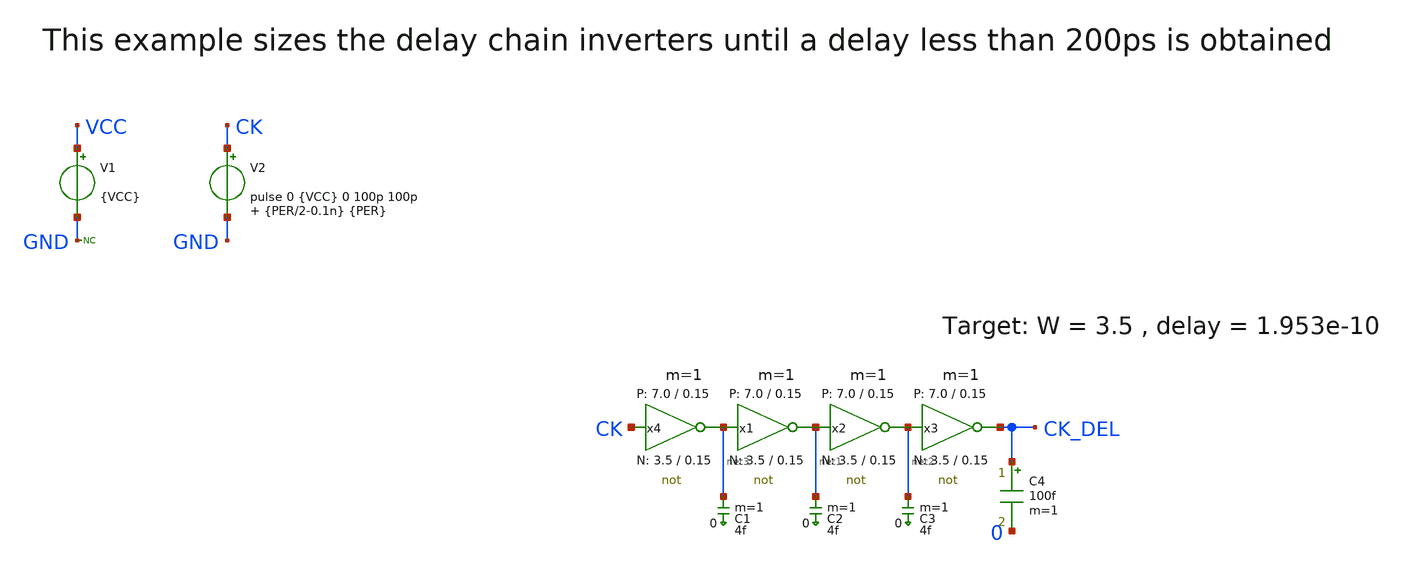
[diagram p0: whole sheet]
** sch_path: sky130A/xschem_libs/sky130_tests/optimize_delay/schematic/optimize_delay.sch
* StefanSchippers/xschem_sky130/sky130_tests/not.sch:
* Copyright 2021 Stefan Frederik Schippers
* Licensed under the Apache License, Version 2.0 (the "License");
.lib $::SKYWATER_MODELS/sky130.lib.spice tt
.include $::SKYWATER_STDCELLS/sky130_fd_sc_hd.spice

**.subckt optimize_delay
V1 VCC GND {VCC}
V2 CK GND pulse 0 {VCC} 0 100p 100p {PER/2-0.1n} {PER}
* noconn GND
C1 net3 0 4f m=1
C2 net1 0 4f m=1
C3 net2 0 4f m=1
x4 net3 CK VCC GND not W_N=3.5 L_N=0.15 W_P=7.0 L_P=0.15 m=1
x1 net1 net3 VCC GND not W_N=3.5 L_N=0.15 W_P=7.0 L_P=0.15 m=1
x2 net2 net1 VCC GND not W_N=3.5 L_N=0.15 W_P=7.0 L_P=0.15 m=1
x3 CK_DEL net2 VCC GND not W_N=3.5 L_N=0.15 W_P=7.0 L_P=0.15 m=1
C4 CK_DEL 0 100f m=1
**** begin user architecture code


.param VCC=1.8
.param FREQ=100e6
.param PER={1/FREQ}
.param ILOAD=100u
.control
  save all
  set nobreak
  set numdgt=3
  set wr_singlescale
  set wr_vecnames
  tran 4p 11n
  write optimize_delay.raw
  * wrdata result.txt ck ck_del
  meas tran del
  + TRIG v(CK) TD=9n VAL=0.9 RISE=1
  + TARG v(CK_DEL) TD=9n VAL=0.9 RISE=1
  print del > result.txt
  quit 0
.endc


**** end user architecture code
**.ends

* expanding   symbol:  sky130_tests/not.sym # of pins=2
** sym_path: sky130_tests/not.sym
** sch_path: sky130_tests/not.sch
.subckt not y a VCCPIN VSSPIN     W_N=1 L_N=0.15 W_P=2 L_P=0.15
*.opin y
*.ipin a
XM1 DN a VSSPIN VSSPIN sky130_fd_pr__nfet_01v8 L=L_N W=W_N nf=1 ad='int((1 + 1)/2) * W_N / 1 * 0.29'
+ as='int((1 + 2)/2) * W_N / 1 * 0.29' pd='2*int((1 + 1)/2) * (W_N / 1 + 0.29)' ps='2*int((1 + 2)/2) * (W_N / 1 + 0.29)'
+ nrd='0.29 / W_N ' nrs='0.29 / W_N ' sa=0 sb=0 sd=0 mult=1 m=1
XM2 DP a VCCPIN VCCPIN sky130_fd_pr__pfet_01v8 L=L_P W=W_P nf=1 ad='int((nf+1)/2) * W/nf * 0.29' as='int((nf+2)/2) * W/nf * 0.29'
+ pd='2*int((nf+1)/2) * (W/nf + 0.29)' ps='2*int((nf+2)/2) * (W/nf + 0.29)' nrd='0.29 / W' nrs='0.29 / W'
+ sa=0 sb=0 sd=0 mult=1 m=1
Vmeas DP y 0
.save i(vmeas)
Vmeas1 y DN 0
.save i(vmeas1)
.save v(dp)
.save v(dn)
.ends

.end
